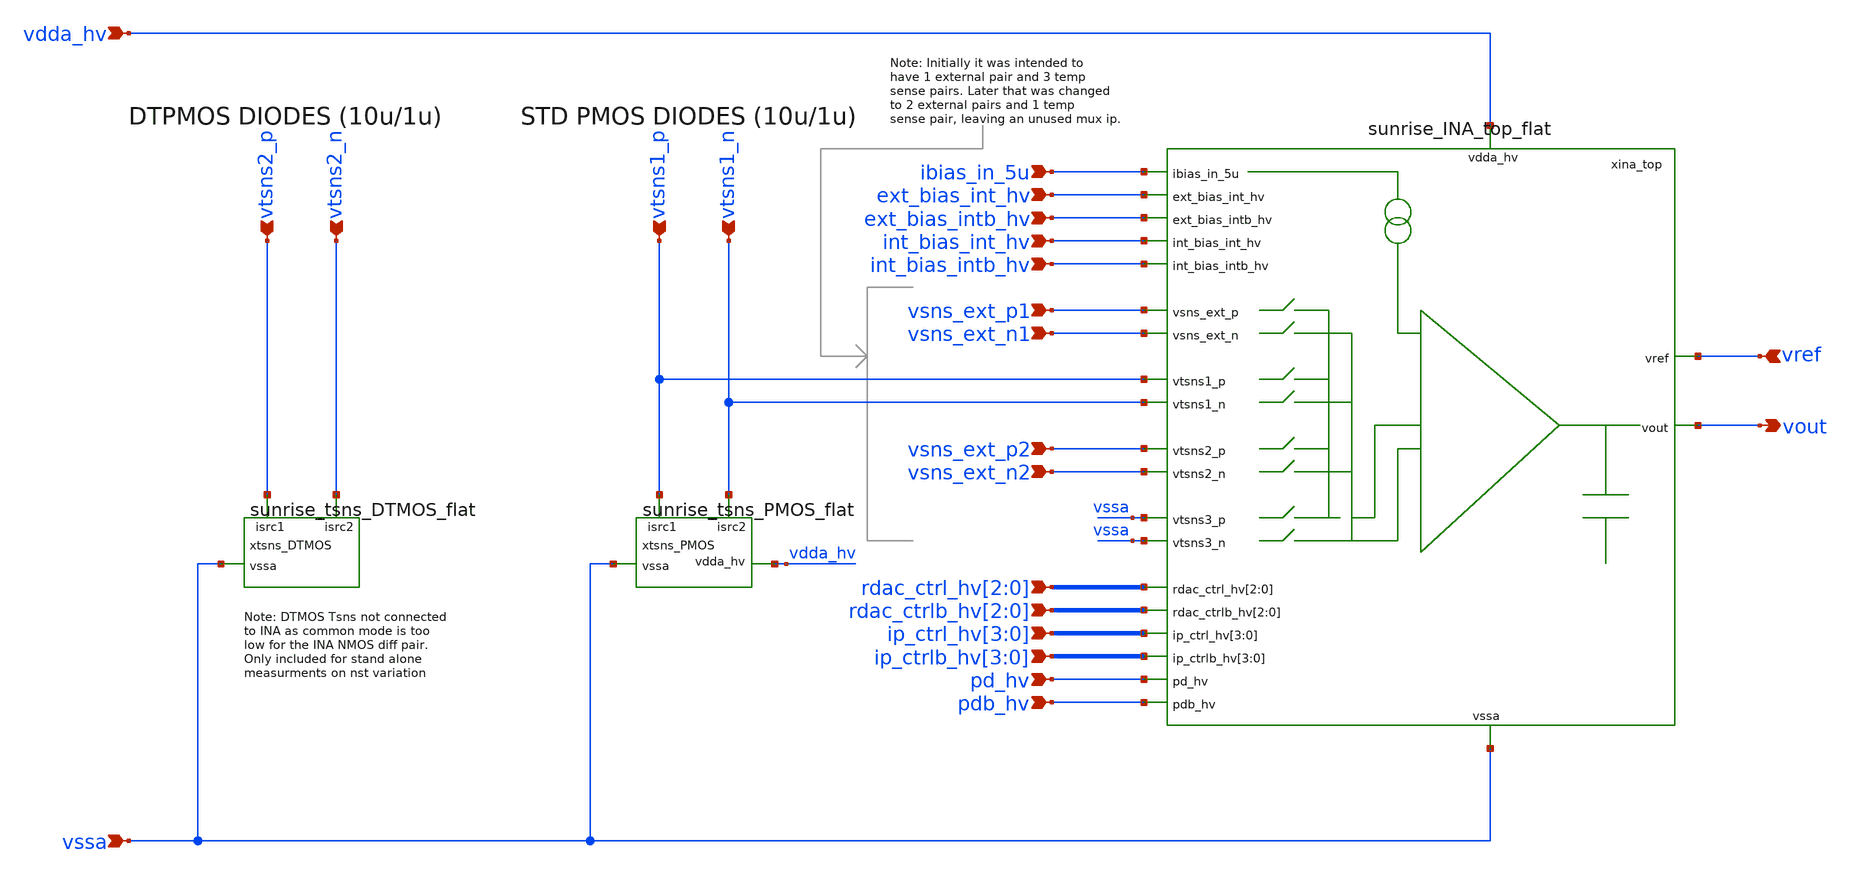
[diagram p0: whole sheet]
** sch_path: Schematics_Layout/sunrise_ina_top_wtsns/sunrise_ina_top_wtsns.sch
**.subckt sunrise_ina_top_wtsns vsns_ext_p1 vsns_ext_n1 vtsns1_p vtsns1_n vsns_ext_p2 vsns_ext_n2
*+ vtsns2_p vtsns2_n ibias_in_5u ext_bias_int_hv ext_bias_intb_hv int_bias_int_hv int_bias_intb_hv
*+ rdac_ctrl_hv[2],rdac_ctrl_hv[1],rdac_ctrl_hv[0] rdac_ctrlb_hv[2],rdac_ctrlb_hv[1],rdac_ctrlb_hv[0]
*+ ip_ctrl_hv[3],ip_ctrl_hv[2],ip_ctrl_hv[1],ip_ctrl_hv[0] ip_ctrlb_hv[3],ip_ctrlb_hv[2],ip_ctrlb_hv[1],ip_ctrlb_hv[0] pd_hv pdb_hv vdda_hv vssa vref vout
*.ipin vsns_ext_p1
*.ipin vsns_ext_n1
*.ipin vtsns1_p
*.ipin vtsns1_n
*.ipin vsns_ext_p2
*.ipin vsns_ext_n2
*.ipin vtsns2_p
*.ipin vtsns2_n
*.ipin ibias_in_5u
*.ipin ext_bias_int_hv
*.ipin ext_bias_intb_hv
*.ipin int_bias_int_hv
*.ipin int_bias_intb_hv
*.ipin rdac_ctrl_hv[2],rdac_ctrl_hv[1],rdac_ctrl_hv[0]
*.ipin rdac_ctrlb_hv[2],rdac_ctrlb_hv[1],rdac_ctrlb_hv[0]
*.ipin ip_ctrl_hv[3],ip_ctrl_hv[2],ip_ctrl_hv[1],ip_ctrl_hv[0]
*.ipin ip_ctrlb_hv[3],ip_ctrlb_hv[2],ip_ctrlb_hv[1],ip_ctrlb_hv[0]
*.ipin pd_hv
*.ipin pdb_hv
*.ipin vdda_hv
*.ipin vssa
*.ipin vref
*.opin vout
xina_top vtsns1_p vtsns1_n vdda_hv vsns_ext_p2 vsns_ext_n2 ibias_in_5u ext_bias_int_hv vssa
+ ext_bias_intb_hv int_bias_int_hv vref int_bias_intb_hv vssa vsns_ext_p1 vout vsns_ext_n1 rdac_ctrl_hv[2]
+ rdac_ctrl_hv[1] rdac_ctrl_hv[0] rdac_ctrlb_hv[2] rdac_ctrlb_hv[1] rdac_ctrlb_hv[0] ip_ctrl_hv[3] ip_ctrl_hv[2]
+ ip_ctrl_hv[1] ip_ctrl_hv[0] ip_ctrlb_hv[3] ip_ctrlb_hv[2] ip_ctrlb_hv[1] ip_ctrlb_hv[0] pd_hv pdb_hv vssa
+ sunrise_INA_top_flat
xtsns_PMOS vtsns1_n vtsns1_p vdda_hv vssa sunrise_tsns_PMOS_flat
xtsns_DTMOS vtsns2_n vtsns2_p vssa sunrise_tsns_DTMOS_flat
**.ends

* expanding   symbol:  sunrise/sunrise_INA_top_flat.sym # of pins=23
** sym_path: Schematics_Layout/sunrise_INA_top/sunrise_INA_top.sym
.include /home/slice/xschem/tb_sunrise_ina_v2/LAYOUT/sunrise_INA_top/PEX/sunrise_INA_top_flat_rcx.spice

* expanding   symbol:  sunrise/sunrise_tsns_PMOS_flat.sym # of pins=4
** sym_path: Schematics_Layout/sunrise_tsns_PMOS/sunrise_tsns_PMOS.sym
.include /home/slice/xschem/tb_sunrise_temp_sense/LAYOUT/sunrise_tsns_PMOS/PEX/sunrise_tsns_PMOS_flat_rcx.spice

* expanding   symbol:  sunrise/sunrise_tsns_DTMOS_flat.sym # of pins=3
** sym_path: Schematics_Layout/sunrise_tsns_DTMOS/sunrise_tsns_DTMOS.sym
.include /home/slice/xschem/tb_sunrise_temp_sense/LAYOUT/sunrise_tsns_DTMOS/PEX/sunrise_tsns_DTMOS_flat_rcx.spice
.end
